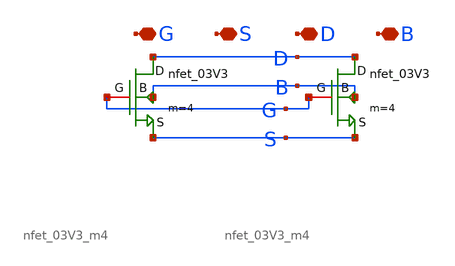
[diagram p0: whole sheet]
** sch_path: DAC_PAKISTAN_01/Pakistan1_Xschem/nfet_03V3_m8.sch
**.subckt nfet_03V3_m8 G S D B
*.iopin G
*.iopin S
*.iopin D
*.iopin B
x1 S D B G nfet_03V3_m4
x2 S D B G nfet_03V3_m4
**.ends
.end
